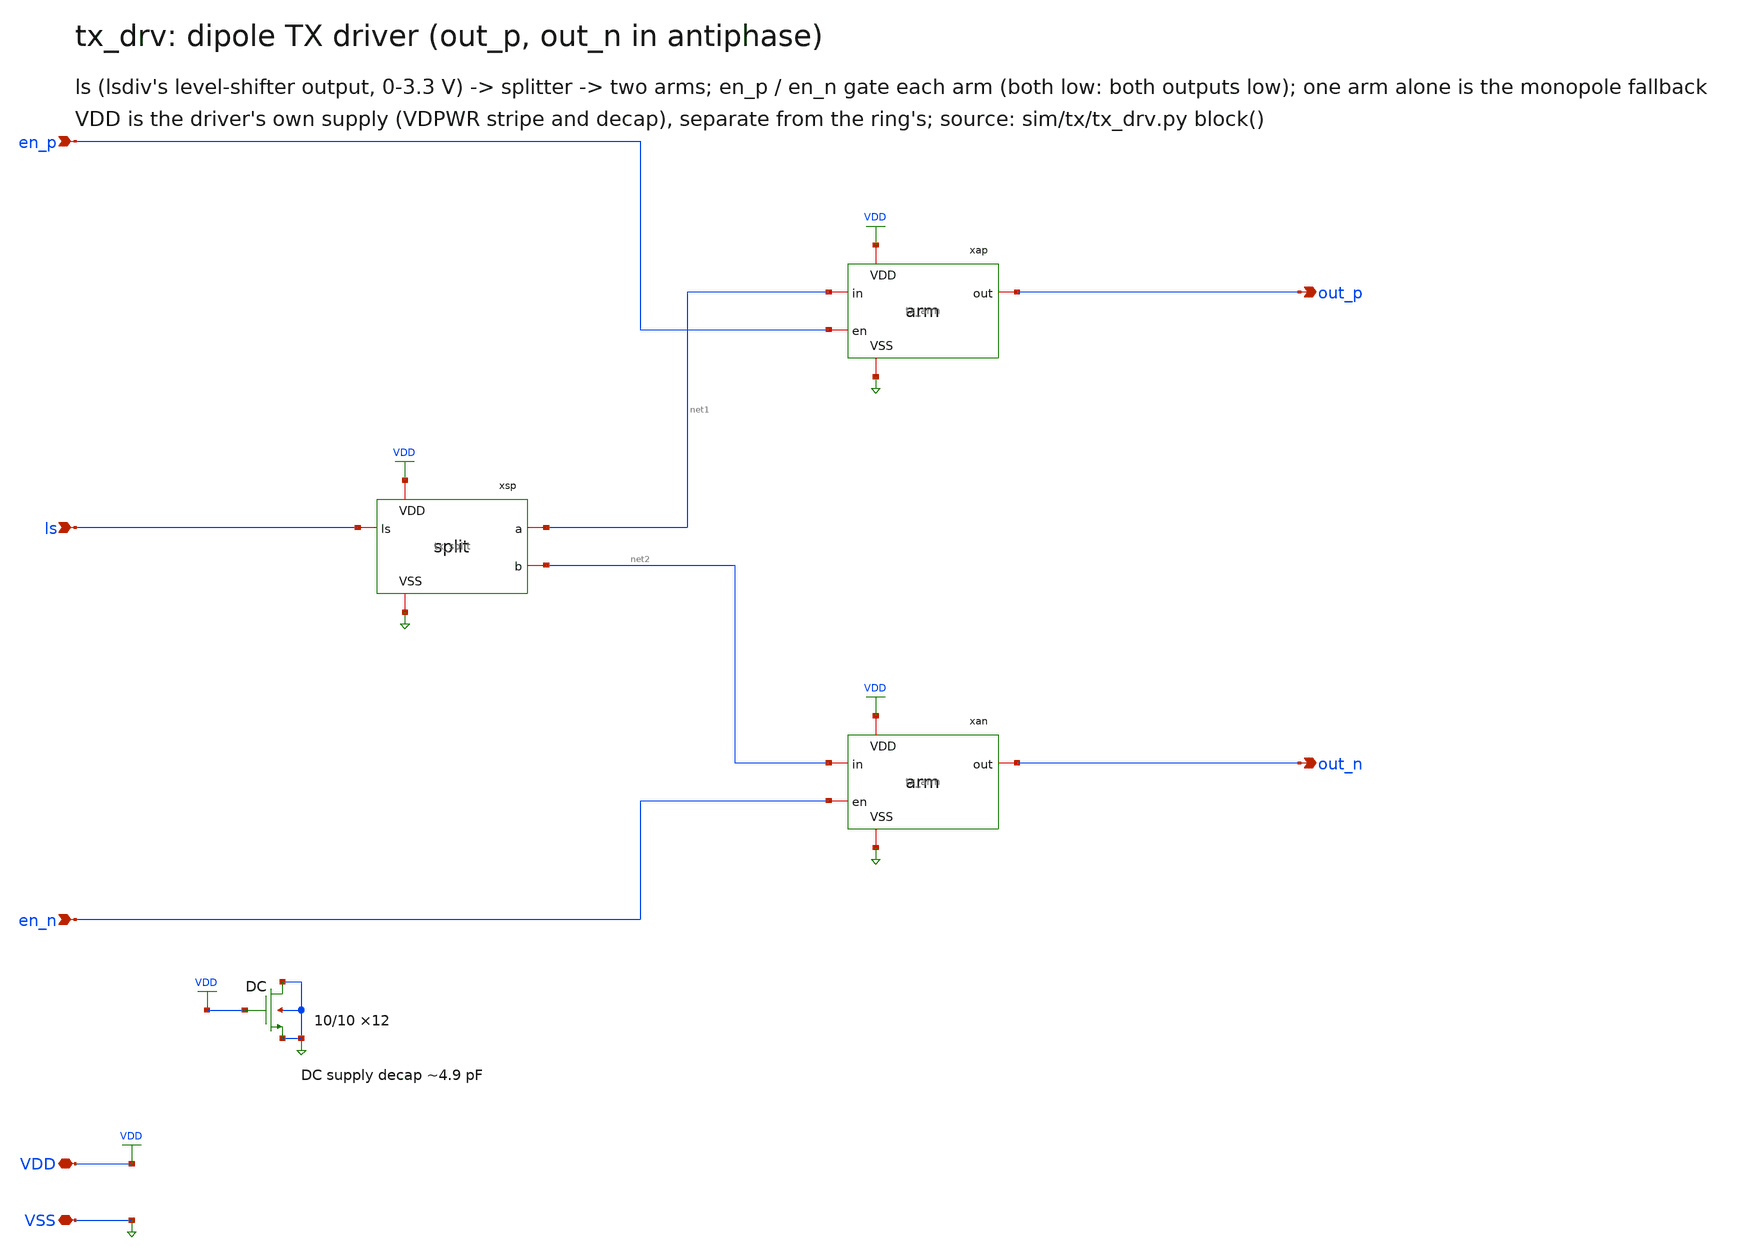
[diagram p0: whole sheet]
** sch_path: xschem/tx_drv.sch
**.subckt tx_drv VDD VSS ls en_p en_n out_p out_n
*.iopin VDD
*.iopin VSS
*.ipin ls
*.ipin en_p
*.ipin en_n
*.opin out_p
*.opin out_n
xsp VDD VSS ls net1 net2 tx_split
xap VDD VSS net1 en_p out_p tx_arm
xan VDD VSS net2 en_n out_n tx_arm
XDC VSS VDD VSS VSS nfet_03v3 L=10.0u W=10.0u nf=1 ad=5.0p as=5.0p pd=21.0u ps=21.0u nrd=0 nrs=0
+ sa=0 sb=0 sd=0 m=12
**.ends

* expanding   symbol:  tx_split.sym # of pins=5
** sym_path: xschem/tx_split.sym
** sch_path: xschem/tx_split.sch
.subckt tx_split VDD VSS ls a b
*.iopin VDD
*.iopin VSS
*.ipin ls
*.opin a
*.opin b
XTp net1 ls VDD VDD pfet_03v3 L=0.28u W=1.0499999999999998u nf=1 ad=0.5249999999999999p
+ as=0.5249999999999999p pd=3.0999999999999996u ps=3.0999999999999996u nrd=0 nrs=0 sa=0 sb=0 sd=0 m=1
XTn net1 ls VSS VSS nfet_03v3 L=0.28u W=0.41999999999999993u nf=1 ad=0.20999999999999996p
+ as=0.20999999999999996p pd=1.8399999999999999u ps=1.8399999999999999u nrd=0 nrs=0 sa=0 sb=0 sd=0 m=1
XA1p net2 net1 VDD VDD pfet_03v3 L=0.28u W=1.25u nf=1 ad=0.625p as=0.625p pd=3.5u ps=3.5u nrd=0
+ nrs=0 sa=0 sb=0 sd=0 m=1
XA1n net2 net1 VSS VSS nfet_03v3 L=0.28u W=0.5u nf=1 ad=0.25p as=0.25p pd=2.0u ps=2.0u nrd=0 nrs=0
+ sa=0 sb=0 sd=0 m=1
XA2p a net2 VDD VDD pfet_03v3 L=0.28u W=2.5u nf=1 ad=1.25p as=1.25p pd=6.0u ps=6.0u nrd=0 nrs=0 sa=0
+ sb=0 sd=0 m=1
XA2n a net2 VSS VSS nfet_03v3 L=0.28u W=1.0u nf=1 ad=0.5p as=0.5p pd=3.0u ps=3.0u nrd=0 nrs=0 sa=0
+ sb=0 sd=0 m=1
XB1p net3 net1 VDD VDD pfet_03v3 L=0.28u W=2.5u nf=1 ad=1.25p as=1.25p pd=6.0u ps=6.0u nrd=0 nrs=0
+ sa=0 sb=0 sd=0 m=1
XB1n net3 net1 VSS VSS nfet_03v3 L=0.28u W=1.0u nf=1 ad=0.5p as=0.5p pd=3.0u ps=3.0u nrd=0 nrs=0
+ sa=0 sb=0 sd=0 m=1
XTGp b VSS net3 VDD pfet_03v3 L=0.28u W=2.5u nf=1 ad=1.25p as=1.25p pd=6.0u ps=6.0u nrd=0 nrs=0 sa=0
+ sb=0 sd=0 m=1
XTGn b VDD net3 VSS nfet_03v3 L=0.28u W=1.0u nf=1 ad=0.5p as=0.5p pd=3.0u ps=3.0u nrd=0 nrs=0 sa=0
+ sb=0 sd=0 m=1
XXBp b a VDD VDD pfet_03v3 L=0.28u W=1.0499999999999998u nf=1 ad=0.5249999999999999p
+ as=0.5249999999999999p pd=3.0999999999999996u ps=3.0999999999999996u nrd=0 nrs=0 sa=0 sb=0 sd=0 m=1
XXBn b a VSS VSS nfet_03v3 L=0.28u W=0.41999999999999993u nf=1 ad=0.20999999999999996p
+ as=0.20999999999999996p pd=1.8399999999999999u ps=1.8399999999999999u nrd=0 nrs=0 sa=0 sb=0 sd=0 m=1
XXAp a b VDD VDD pfet_03v3 L=0.28u W=1.0499999999999998u nf=1 ad=0.5249999999999999p
+ as=0.5249999999999999p pd=3.0999999999999996u ps=3.0999999999999996u nrd=0 nrs=0 sa=0 sb=0 sd=0 m=1
XXAn a b VSS VSS nfet_03v3 L=0.28u W=0.41999999999999993u nf=1 ad=0.20999999999999996p
+ as=0.20999999999999996p pd=1.8399999999999999u ps=1.8399999999999999u nrd=0 nrs=0 sa=0 sb=0 sd=0 m=1
.ends


* expanding   symbol:  tx_arm.sym # of pins=5
** sym_path: xschem/tx_arm.sym
** sch_path: xschem/tx_arm.sch
.subckt tx_arm VDD VSS in en out
*.iopin VDD
*.iopin VSS
*.ipin in
*.ipin en
*.opin out
XNAp net1 in VDD VDD pfet_03v3 L=0.28u W=1.25u nf=1 ad=0.625p as=0.625p pd=3.5u ps=3.5u nrd=0 nrs=0
+ sa=0 sb=0 sd=0 m=1
XNBp net1 en VDD VDD pfet_03v3 L=0.28u W=1.25u nf=1 ad=0.625p as=0.625p pd=3.5u ps=3.5u nrd=0 nrs=0
+ sa=0 sb=0 sd=0 m=1
XNAn net1 in net2 VSS nfet_03v3 L=0.28u W=1.0u nf=1 ad=0.5p as=0.5p pd=3.0u ps=3.0u nrd=0 nrs=0 sa=0
+ sb=0 sd=0 m=1
XNBn net2 en VSS VSS nfet_03v3 L=0.28u W=1.0u nf=1 ad=0.5p as=0.5p pd=3.0u ps=3.0u nrd=0 nrs=0 sa=0
+ sb=0 sd=0 m=1
XM1p net3 net1 VDD VDD pfet_03v3 L=0.28u W=1.0499999999999998u nf=1 ad=0.5249999999999999p
+ as=0.5249999999999999p pd=3.0999999999999996u ps=3.0999999999999996u nrd=0 nrs=0 sa=0 sb=0 sd=0 m=1
XM1n net3 net1 VSS VSS nfet_03v3 L=0.28u W=0.41999999999999993u nf=1 ad=0.20999999999999996p
+ as=0.20999999999999996p pd=1.8399999999999999u ps=1.8399999999999999u nrd=0 nrs=0 sa=0 sb=0 sd=0 m=1
XM2p net4 net3 VDD VDD pfet_03v3 L=0.28u W=1.5624999999999998u nf=1 ad=0.7812499999999999p
+ as=0.7812499999999999p pd=4.125u ps=4.125u nrd=0 nrs=0 sa=0 sb=0 sd=0 m=1
XM2n net4 net3 VSS VSS nfet_03v3 L=0.28u W=0.625u nf=1 ad=0.3125p as=0.3125p pd=2.25u ps=2.25u nrd=0
+ nrs=0 sa=0 sb=0 sd=0 m=1
XM3p net5 net4 VDD VDD pfet_03v3 L=0.28u W=6.249999999999999u nf=1 ad=3.1249999999999996p
+ as=3.1249999999999996p pd=13.499999999999998u ps=13.499999999999998u nrd=0 nrs=0 sa=0 sb=0 sd=0 m=1
XM3n net5 net4 VSS VSS nfet_03v3 L=0.28u W=2.5u nf=1 ad=1.25p as=1.25p pd=6.0u ps=6.0u nrd=0 nrs=0
+ sa=0 sb=0 sd=0 m=1
XM4p net6 net5 VDD VDD pfet_03v3 L=0.28u W=24.999999999999996u nf=1 ad=12.499999999999998p
+ as=12.499999999999998p pd=50.99999999999999u ps=50.99999999999999u nrd=0 nrs=0 sa=0 sb=0 sd=0 m=1
XM4n net6 net5 VSS VSS nfet_03v3 L=0.28u W=10.0u nf=1 ad=5.0p as=5.0p pd=21.0u ps=21.0u nrd=0 nrs=0
+ sa=0 sb=0 sd=0 m=1
XM5p out net6 VDD VDD pfet_03v3 L=0.28u W=99.99999999999999u nf=1 ad=49.99999999999999p
+ as=49.99999999999999p pd=200.99999999999997u ps=200.99999999999997u nrd=0 nrs=0 sa=0 sb=0 sd=0 m=1
XM5n out net6 VSS VSS nfet_03v3 L=0.28u W=40.0u nf=1 ad=20.0p as=20.0p pd=81.0u ps=81.0u nrd=0 nrs=0
+ sa=0 sb=0 sd=0 m=1
.ends

.end
